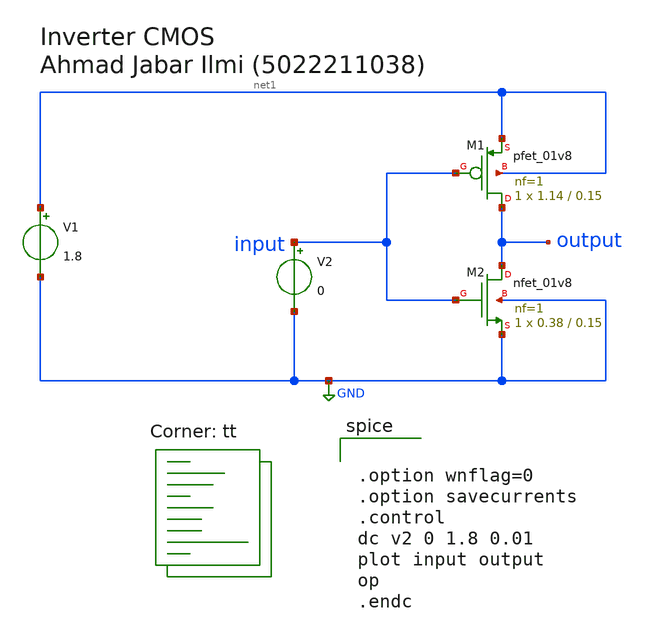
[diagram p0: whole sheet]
** sch_path: invertercmos/invertercmos.sch
**.subckt invertercmos
XM1 output input net1 net1 sky130_fd_pr__pfet_01v8 L=0.15 W=1.14 nf=1 ad='int((nf+1)/2) * W/nf * 0.29'
+ as='int((nf+2)/2) * W/nf * 0.29' pd='2*int((nf+1)/2) * (W/nf + 0.29)' ps='2*int((nf+2)/2) * (W/nf + 0.29)'
+ nrd='0.29 / W' nrs='0.29 / W' sa=0 sb=0 sd=0 mult=1 m=1
XM2 output input GND GND sky130_fd_pr__nfet_01v8 L=0.15 W=0.38 nf=1 ad='int((nf+1)/2) * W/nf * 0.29'
+ as='int((nf+2)/2) * W/nf * 0.29' pd='2*int((nf+1)/2) * (W/nf + 0.29)' ps='2*int((nf+2)/2) * (W/nf + 0.29)'
+ nrd='0.29 / W' nrs='0.29 / W' sa=0 sb=0 sd=0 mult=1 m=1
V1 net1 GND 1.8
V2 input GND 0
**** begin user architecture code
.lib $::SKYWATER_MODELS/sky130.lib.spice tt


.option wnflag=0
.option savecurrents
.control
dc v2 0 1.8 0.01
plot input output
op
.endc


**** end user architecture code
**.ends
.GLOBAL GND
.end
